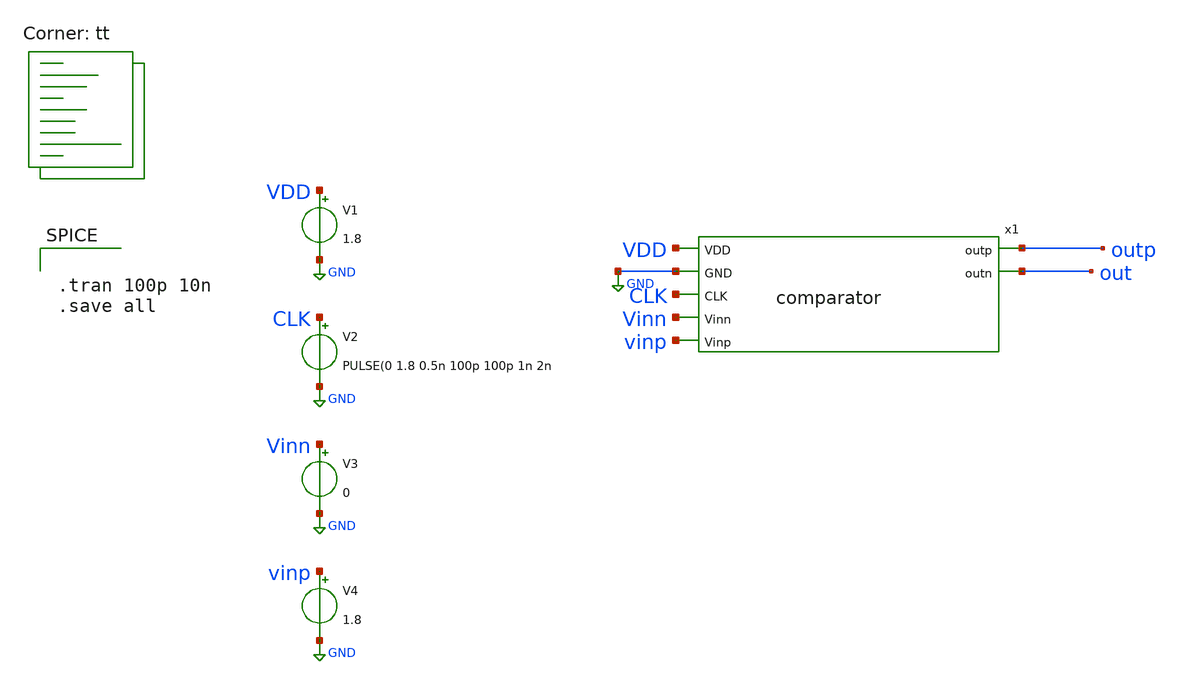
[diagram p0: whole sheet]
** sch_path: xschem/comp_test.sch
**.subckt comp_test
x1 VDD GND CLK outp out Vinn vinp comparator
V2 CLK GND PULSE(0 1.8 0.5n 100p 100p 1n 2n
V1 VDD GND 1.8
V3 Vinn GND 0
V4 vinp GND 1.8
**** begin user architecture code
.lib $::SKYWATER_MODELS/sky130.lib.spice tt


.tran 100p 10n
.save all


**** end user architecture code
**.ends
.GLOBAL GND
.end
